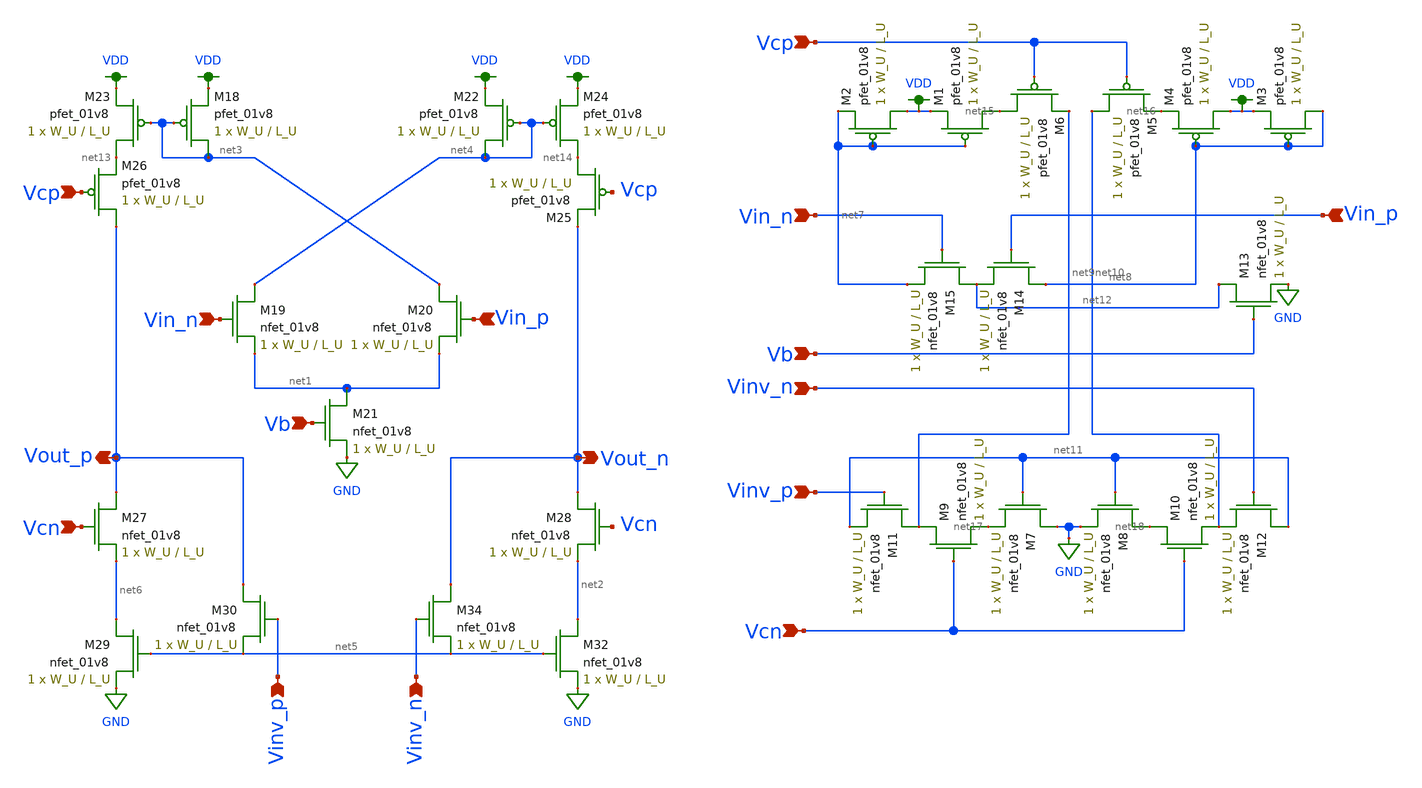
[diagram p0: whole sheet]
** sch_path: schematics/ota_lds.sch
**.subckt ota_lds Vin_n Vin_p Vout_n Vout_p Vcp Vb Vinv_p Vinv_n Vcn Vcp Vcn Vinv_p Vinv_n Vb Vin_n
*+ Vin_p
*.ipin Vin_n
*.ipin Vin_p
*.opin Vout_n
*.opin Vout_p
*.ipin Vcp
*.ipin Vb
*.ipin Vinv_p
*.ipin Vinv_n
*.ipin Vcn
*.ipin Vcp
*.ipin Vcn
*.ipin Vinv_p
*.ipin Vinv_n
*.ipin Vb
*.ipin Vin_n
*.ipin Vin_p
XM18 net3 net3 VDD VDD sky130_fd_pr__pfet_01v8 L=L_U W=W_U nf=1 ad='int((nf+1)/2) * W/nf * 0.29' as='int((nf+2)/2) * W/nf * 0.29'
+ pd='2*int((nf+1)/2) * (W/nf + 0.29)' ps='2*int((nf+2)/2) * (W/nf + 0.29)' nrd='0.29 / W' nrs='0.29 / W'
+ sa=0 sb=0 sd=0 mult=1 m=1
XM19 net4 Vin_n net1 GND sky130_fd_pr__nfet_01v8 L=L_U W=W_U nf=1 ad='int((nf+1)/2) * W/nf * 0.29' as='int((nf+2)/2) * W/nf * 0.29'
+ pd='2*int((nf+1)/2) * (W/nf + 0.29)' ps='2*int((nf+2)/2) * (W/nf + 0.29)' nrd='0.29 / W' nrs='0.29 / W'
+ sa=0 sb=0 sd=0 mult=1 m=1
XM20 net3 Vin_p net1 GND sky130_fd_pr__nfet_01v8 L=L_U W=W_U nf=1 ad='int((nf+1)/2) * W/nf * 0.29' as='int((nf+2)/2) * W/nf * 0.29'
+ pd='2*int((nf+1)/2) * (W/nf + 0.29)' ps='2*int((nf+2)/2) * (W/nf + 0.29)' nrd='0.29 / W' nrs='0.29 / W'
+ sa=0 sb=0 sd=0 mult=1 m=1
XM21 net1 Vb GND GND sky130_fd_pr__nfet_01v8 L=L_U W=W_U nf=1 ad='int((nf+1)/2) * W/nf * 0.29' as='int((nf+2)/2) * W/nf * 0.29'
+ pd='2*int((nf+1)/2) * (W/nf + 0.29)' ps='2*int((nf+2)/2) * (W/nf + 0.29)' nrd='0.29 / W' nrs='0.29 / W'
+ sa=0 sb=0 sd=0 mult=1 m=1
XM22 net4 net4 VDD VDD sky130_fd_pr__pfet_01v8 L=L_U W=W_U nf=1 ad='int((nf+1)/2) * W/nf * 0.29' as='int((nf+2)/2) * W/nf * 0.29'
+ pd='2*int((nf+1)/2) * (W/nf + 0.29)' ps='2*int((nf+2)/2) * (W/nf + 0.29)' nrd='0.29 / W' nrs='0.29 / W'
+ sa=0 sb=0 sd=0 mult=1 m=1
XM23 net13 net3 VDD VDD sky130_fd_pr__pfet_01v8 L=L_U W=W_U nf=1 ad='int((nf+1)/2) * W/nf * 0.29' as='int((nf+2)/2) * W/nf * 0.29'
+ pd='2*int((nf+1)/2) * (W/nf + 0.29)' ps='2*int((nf+2)/2) * (W/nf + 0.29)' nrd='0.29 / W' nrs='0.29 / W'
+ sa=0 sb=0 sd=0 mult=1 m=1
XM24 net14 net4 VDD VDD sky130_fd_pr__pfet_01v8 L=L_U W=W_U nf=1 ad='int((nf+1)/2) * W/nf * 0.29' as='int((nf+2)/2) * W/nf * 0.29'
+ pd='2*int((nf+1)/2) * (W/nf + 0.29)' ps='2*int((nf+2)/2) * (W/nf + 0.29)' nrd='0.29 / W' nrs='0.29 / W'
+ sa=0 sb=0 sd=0 mult=1 m=1
XM25 net14 Vcp Vout_n VDD sky130_fd_pr__pfet_01v8 L=L_U W=W_U nf=1 ad='int((nf+1)/2) * W/nf * 0.29' as='int((nf+2)/2) * W/nf * 0.29'
+ pd='2*int((nf+1)/2) * (W/nf + 0.29)' ps='2*int((nf+2)/2) * (W/nf + 0.29)' nrd='0.29 / W' nrs='0.29 / W'
+ sa=0 sb=0 sd=0 mult=1 m=1
XM26 Vout_p Vcp net13 VDD sky130_fd_pr__pfet_01v8 L=L_U W=W_U nf=1 ad='int((nf+1)/2) * W/nf * 0.29' as='int((nf+2)/2) * W/nf * 0.29'
+ pd='2*int((nf+1)/2) * (W/nf + 0.29)' ps='2*int((nf+2)/2) * (W/nf + 0.29)' nrd='0.29 / W' nrs='0.29 / W'
+ sa=0 sb=0 sd=0 mult=1 m=1
XM27 Vout_p Vcn net6 GND sky130_fd_pr__nfet_01v8 L=L_U W=W_U nf=1 ad='int((nf+1)/2) * W/nf * 0.29' as='int((nf+2)/2) * W/nf * 0.29'
+ pd='2*int((nf+1)/2) * (W/nf + 0.29)' ps='2*int((nf+2)/2) * (W/nf + 0.29)' nrd='0.29 / W' nrs='0.29 / W'
+ sa=0 sb=0 sd=0 mult=1 m=1
XM28 Vout_n Vcn net2 GND sky130_fd_pr__nfet_01v8 L=L_U W=W_U nf=1 ad='int((nf+1)/2) * W/nf * 0.29' as='int((nf+2)/2) * W/nf * 0.29'
+ pd='2*int((nf+1)/2) * (W/nf + 0.29)' ps='2*int((nf+2)/2) * (W/nf + 0.29)' nrd='0.29 / W' nrs='0.29 / W'
+ sa=0 sb=0 sd=0 mult=1 m=1
XM29 net6 net5 GND GND sky130_fd_pr__nfet_01v8 L=L_U W=W_U nf=1 ad='int((nf+1)/2) * W/nf * 0.29' as='int((nf+2)/2) * W/nf * 0.29'
+ pd='2*int((nf+1)/2) * (W/nf + 0.29)' ps='2*int((nf+2)/2) * (W/nf + 0.29)' nrd='0.29 / W' nrs='0.29 / W'
+ sa=0 sb=0 sd=0 mult=1 m=1
XM30 Vout_p Vinv_p net5 GND sky130_fd_pr__nfet_01v8 L=L_U W=W_U nf=1 ad='int((nf+1)/2) * W/nf * 0.29'
+ as='int((nf+2)/2) * W/nf * 0.29' pd='2*int((nf+1)/2) * (W/nf + 0.29)' ps='2*int((nf+2)/2) * (W/nf + 0.29)'
+ nrd='0.29 / W' nrs='0.29 / W' sa=0 sb=0 sd=0 mult=1 m=1
XM32 net2 net5 GND GND sky130_fd_pr__nfet_01v8 L=L_U W=W_U nf=1 ad='int((nf+1)/2) * W/nf * 0.29' as='int((nf+2)/2) * W/nf * 0.29'
+ pd='2*int((nf+1)/2) * (W/nf + 0.29)' ps='2*int((nf+2)/2) * (W/nf + 0.29)' nrd='0.29 / W' nrs='0.29 / W'
+ sa=0 sb=0 sd=0 mult=1 m=1
XM34 Vout_n Vinv_n net5 GND sky130_fd_pr__nfet_01v8 L=L_U W=W_U nf=1 ad='int((nf+1)/2) * W/nf * 0.29'
+ as='int((nf+2)/2) * W/nf * 0.29' pd='2*int((nf+1)/2) * (W/nf + 0.29)' ps='2*int((nf+2)/2) * (W/nf + 0.29)'
+ nrd='0.29 / W' nrs='0.29 / W' sa=0 sb=0 sd=0 mult=1 m=1
XM1 net15 net7 VDD VDD sky130_fd_pr__pfet_01v8 L=L_U W=W_U nf=1 ad='int((nf+1)/2) * W/nf * 0.29' as='int((nf+2)/2) * W/nf * 0.29'
+ pd='2*int((nf+1)/2) * (W/nf + 0.29)' ps='2*int((nf+2)/2) * (W/nf + 0.29)' nrd='0.29 / W' nrs='0.29 / W'
+ sa=0 sb=0 sd=0 mult=1 m=1
XM2 VDD net7 net7 VDD sky130_fd_pr__pfet_01v8 L=L_U W=W_U nf=1 ad='int((nf+1)/2) * W/nf * 0.29' as='int((nf+2)/2) * W/nf * 0.29'
+ pd='2*int((nf+1)/2) * (W/nf + 0.29)' ps='2*int((nf+2)/2) * (W/nf + 0.29)' nrd='0.29 / W' nrs='0.29 / W'
+ sa=0 sb=0 sd=0 mult=1 m=1
XM3 net8 net8 VDD VDD sky130_fd_pr__pfet_01v8 L=L_U W=W_U nf=1 ad='int((nf+1)/2) * W/nf * 0.29' as='int((nf+2)/2) * W/nf * 0.29'
+ pd='2*int((nf+1)/2) * (W/nf + 0.29)' ps='2*int((nf+2)/2) * (W/nf + 0.29)' nrd='0.29 / W' nrs='0.29 / W'
+ sa=0 sb=0 sd=0 mult=1 m=1
XM4 VDD net8 net16 VDD sky130_fd_pr__pfet_01v8 L=L_U W=W_U nf=1 ad='int((nf+1)/2) * W/nf * 0.29' as='int((nf+2)/2) * W/nf * 0.29'
+ pd='2*int((nf+1)/2) * (W/nf + 0.29)' ps='2*int((nf+2)/2) * (W/nf + 0.29)' nrd='0.29 / W' nrs='0.29 / W'
+ sa=0 sb=0 sd=0 mult=1 m=1
XM5 net10 Vcp net16 VDD sky130_fd_pr__pfet_01v8 L=L_U W=W_U nf=1 ad='int((nf+1)/2) * W/nf * 0.29' as='int((nf+2)/2) * W/nf * 0.29'
+ pd='2*int((nf+1)/2) * (W/nf + 0.29)' ps='2*int((nf+2)/2) * (W/nf + 0.29)' nrd='0.29 / W' nrs='0.29 / W'
+ sa=0 sb=0 sd=0 mult=1 m=1
XM6 net15 Vcp net9 VDD sky130_fd_pr__pfet_01v8 L=L_U W=W_U nf=1 ad='int((nf+1)/2) * W/nf * 0.29' as='int((nf+2)/2) * W/nf * 0.29'
+ pd='2*int((nf+1)/2) * (W/nf + 0.29)' ps='2*int((nf+2)/2) * (W/nf + 0.29)' nrd='0.29 / W' nrs='0.29 / W'
+ sa=0 sb=0 sd=0 mult=1 m=1
XM7 GND net11 net17 GND sky130_fd_pr__nfet_01v8 L=L_U W=W_U nf=1 ad='int((nf+1)/2) * W/nf * 0.29' as='int((nf+2)/2) * W/nf * 0.29'
+ pd='2*int((nf+1)/2) * (W/nf + 0.29)' ps='2*int((nf+2)/2) * (W/nf + 0.29)' nrd='0.29 / W' nrs='0.29 / W'
+ sa=0 sb=0 sd=0 mult=1 m=1
XM8 net18 net11 GND GND sky130_fd_pr__nfet_01v8 L=L_U W=W_U nf=1 ad='int((nf+1)/2) * W/nf * 0.29' as='int((nf+2)/2) * W/nf * 0.29'
+ pd='2*int((nf+1)/2) * (W/nf + 0.29)' ps='2*int((nf+2)/2) * (W/nf + 0.29)' nrd='0.29 / W' nrs='0.29 / W'
+ sa=0 sb=0 sd=0 mult=1 m=1
XM9 net9 Vcn net17 GND sky130_fd_pr__nfet_01v8 L=L_U W=W_U nf=1 ad='int((nf+1)/2) * W/nf * 0.29' as='int((nf+2)/2) * W/nf * 0.29'
+ pd='2*int((nf+1)/2) * (W/nf + 0.29)' ps='2*int((nf+2)/2) * (W/nf + 0.29)' nrd='0.29 / W' nrs='0.29 / W'
+ sa=0 sb=0 sd=0 mult=1 m=1
XM10 net18 Vcn net10 GND sky130_fd_pr__nfet_01v8 L=L_U W=W_U nf=1 ad='int((nf+1)/2) * W/nf * 0.29' as='int((nf+2)/2) * W/nf * 0.29'
+ pd='2*int((nf+1)/2) * (W/nf + 0.29)' ps='2*int((nf+2)/2) * (W/nf + 0.29)' nrd='0.29 / W' nrs='0.29 / W'
+ sa=0 sb=0 sd=0 mult=1 m=1
XM11 net9 Vinv_p net11 GND sky130_fd_pr__nfet_01v8 L=L_U W=W_U nf=1 ad='int((nf+1)/2) * W/nf * 0.29'
+ as='int((nf+2)/2) * W/nf * 0.29' pd='2*int((nf+1)/2) * (W/nf + 0.29)' ps='2*int((nf+2)/2) * (W/nf + 0.29)'
+ nrd='0.29 / W' nrs='0.29 / W' sa=0 sb=0 sd=0 mult=1 m=1
XM12 net11 Vinv_n net10 GND sky130_fd_pr__nfet_01v8 L=L_U W=W_U nf=1 ad='int((nf+1)/2) * W/nf * 0.29'
+ as='int((nf+2)/2) * W/nf * 0.29' pd='2*int((nf+1)/2) * (W/nf + 0.29)' ps='2*int((nf+2)/2) * (W/nf + 0.29)'
+ nrd='0.29 / W' nrs='0.29 / W' sa=0 sb=0 sd=0 mult=1 m=1
XM13 net12 Vb GND GND sky130_fd_pr__nfet_01v8 L=L_U W=W_U nf=1 ad='int((nf+1)/2) * W/nf * 0.29' as='int((nf+2)/2) * W/nf * 0.29'
+ pd='2*int((nf+1)/2) * (W/nf + 0.29)' ps='2*int((nf+2)/2) * (W/nf + 0.29)' nrd='0.29 / W' nrs='0.29 / W'
+ sa=0 sb=0 sd=0 mult=1 m=1
XM14 net8 Vin_p net12 GND sky130_fd_pr__nfet_01v8 L=L_U W=W_U nf=1 ad='int((nf+1)/2) * W/nf * 0.29' as='int((nf+2)/2) * W/nf * 0.29'
+ pd='2*int((nf+1)/2) * (W/nf + 0.29)' ps='2*int((nf+2)/2) * (W/nf + 0.29)' nrd='0.29 / W' nrs='0.29 / W'
+ sa=0 sb=0 sd=0 mult=1 m=1
XM15 net12 Vin_n net7 GND sky130_fd_pr__nfet_01v8 L=L_U W=W_U nf=1 ad='int((nf+1)/2) * W/nf * 0.29' as='int((nf+2)/2) * W/nf * 0.29'
+ pd='2*int((nf+1)/2) * (W/nf + 0.29)' ps='2*int((nf+2)/2) * (W/nf + 0.29)' nrd='0.29 / W' nrs='0.29 / W'
+ sa=0 sb=0 sd=0 mult=1 m=1
**.ends
.GLOBAL VDD
.GLOBAL GND
.end
